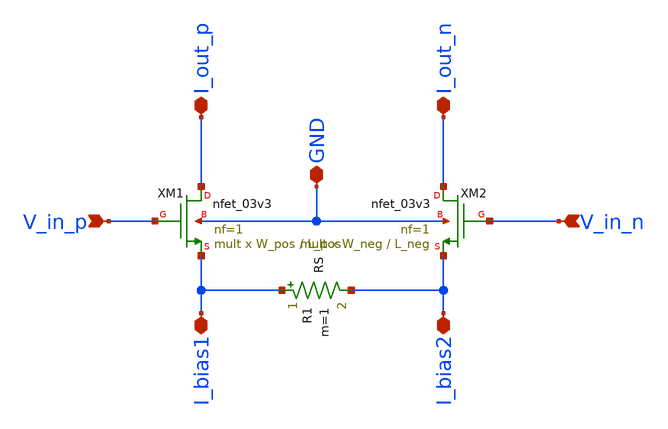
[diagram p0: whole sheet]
** sch_path: src/design_xsch/experimental_hierarchal/diff_pair_with_source_degeneration.sch
**.subckt diff_pair_with_source_degeneration V_in_p V_in_n I_out_p I_out_n I_bias1 I_bias2 GND
*.ipin V_in_p
*.ipin V_in_n
*.iopin I_out_p
*.iopin I_out_n
*.iopin I_bias1
*.iopin I_bias2
*.iopin GND
XM1 I_out_p V_in_p I_bias1 GND nfet_03v3 L=L_pos W=W_pos nf=1 ad='int((nf+1)/2) * W/nf * 0.18u' as='int((nf+2)/2) * W/nf * 0.18u'
+ pd='2*int((nf+1)/2) * (W/nf + 0.18u)' ps='2*int((nf+2)/2) * (W/nf + 0.18u)' nrd='0.18u / W' nrs='0.18u / W'
+ sa=0 sb=0 sd=0 m=mult
XM2 I_out_n V_in_n I_bias2 GND nfet_03v3 L=L_neg W=W_neg nf=1 ad='int((nf+1)/2) * W/nf * 0.18u' as='int((nf+2)/2) * W/nf * 0.18u'
+ pd='2*int((nf+1)/2) * (W/nf + 0.18u)' ps='2*int((nf+2)/2) * (W/nf + 0.18u)' nrd='0.18u / W' nrs='0.18u / W'
+ sa=0 sb=0 sd=0 m=mult
R1 I_bias1 I_bias2 RS m=1
**.ends
.end
